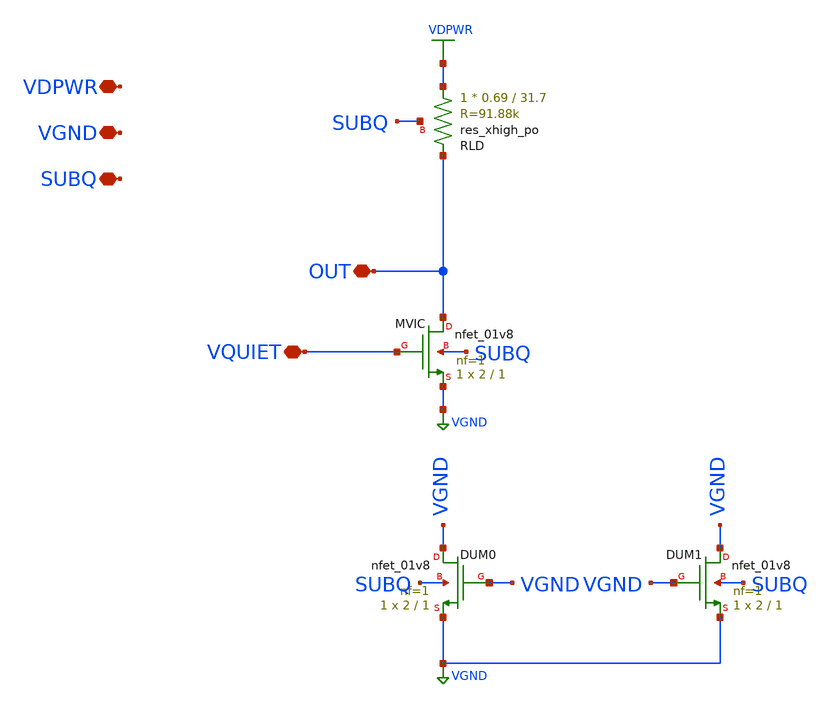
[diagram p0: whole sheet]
** sch_path: cells/ELAD1_VICTIM_BASELINE/schematic/ELAD1_VICTIM_BASELINE.sch
**.subckt ELAD1_VICTIM_BASELINE VQUIET OUT VDPWR VGND SUBQ
*.iopin VQUIET
*.iopin OUT
*.iopin VDPWR
*.iopin VGND
*.iopin SUBQ
XMVIC OUT VQUIET VGND SUBQ sky130_fd_pr__nfet_01v8 L=1 W=2 nf=1 ad='int((1 + 1)/2) * 2 / 1 * 0.29' as='int((1 + 2)/2) * 2 / 1 * 0.29'
+ pd='2*int((1 + 1)/2) * (2 / 1 + 0.29)' ps='2*int((1 + 2)/2) * (2 / 1 + 0.29)' nrd='0.29 / 2 ' nrs='0.29 / 2 '
+ sa=0 sb=0 sd=0 mult=1 m=1
XRLD VDPWR OUT SUBQ sky130_fd_pr__res_xhigh_po W=0.69 L=31.7 mult=1 m=1
XDUM0 VGND VGND VGND SUBQ sky130_fd_pr__nfet_01v8 L=1 W=2 nf=1 ad='int((1 + 1)/2) * 2 / 1 * 0.29' as='int((1 + 2)/2) * 2 / 1 * 0.29'
+ pd='2*int((1 + 1)/2) * (2 / 1 + 0.29)' ps='2*int((1 + 2)/2) * (2 / 1 + 0.29)' nrd='0.29 / 2 ' nrs='0.29 / 2 '
+ sa=0 sb=0 sd=0 mult=1 m=1
XDUM1 VGND VGND VGND SUBQ sky130_fd_pr__nfet_01v8 L=1 W=2 nf=1 ad='int((1 + 1)/2) * 2 / 1 * 0.29' as='int((1 + 2)/2) * 2 / 1 * 0.29'
+ pd='2*int((1 + 1)/2) * (2 / 1 + 0.29)' ps='2*int((1 + 2)/2) * (2 / 1 + 0.29)' nrd='0.29 / 2 ' nrs='0.29 / 2 '
+ sa=0 sb=0 sd=0 mult=1 m=1
**.ends
.GLOBAL VGND
.GLOBAL VDPWR
.end
